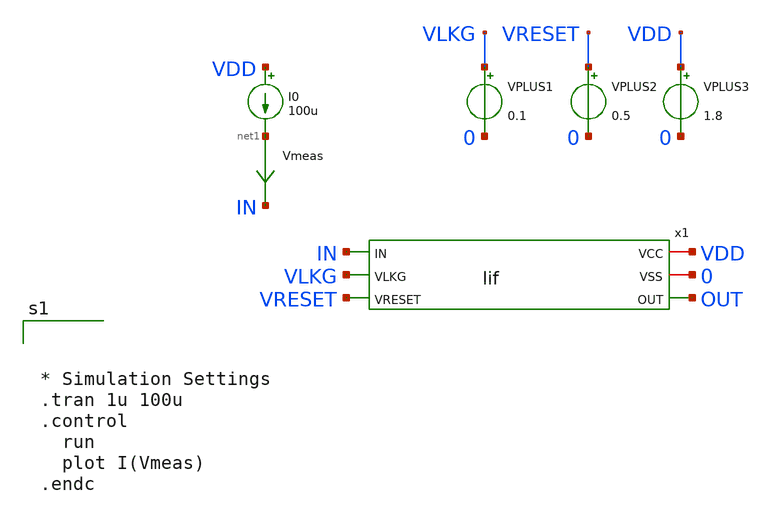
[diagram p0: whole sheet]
** sch_path: xschem/tb_lif.sch
**.subckt tb_lif
VPLUS1 VLKG 0 0.1
VPLUS2 VRESET 0 0.5
VPLUS3 VDD 0 1.8
x1 VDD 0 IN OUT VLKG VRESET lif
I0 VDD net1 100u
Vmeas net1 IN 0
.save i(vmeas)
**** begin user architecture code

** opencircuitdesign pdks install
.lib $::SKYWATER_MODELS/sky130.lib.spice tt





* Simulation Settings
.tran 1u 100u
.control
  run
  plot I(Vmeas)
.endc


**** end user architecture code
**.ends

* expanding   symbol:  lif.sym # of pins=6
** sym_path: xschem/lif.sym
** sch_path: xschem/lif.sch
.subckt lif VCC VSS IN OUT VLKG VRESET
*.iopin VCC
*.iopin VSS
*.ipin IN
*.opin OUT
*.ipin VLKG
*.ipin VRESET
XM1 IN VLKG VSS VSS sky130_fd_pr__nfet_01v8 L=0.15 W=1 nf=1 ad='int((nf+1)/2) * W/nf * 0.29' as='int((nf+2)/2) * W/nf * 0.29'
+ pd='2*int((nf+1)/2) * (W/nf + 0.29)' ps='2*int((nf+2)/2) * (W/nf + 0.29)' nrd='0.29 / W' nrs='0.29 / W'
+ sa=0 sb=0 sd=0 mult=1 m=1
XM2 IN OUT VRESET VSS sky130_fd_pr__nfet_01v8 L=0.15 W=1 nf=1 ad='int((nf+1)/2) * W/nf * 0.29' as='int((nf+2)/2) * W/nf * 0.29'
+ pd='2*int((nf+1)/2) * (W/nf + 0.29)' ps='2*int((nf+2)/2) * (W/nf + 0.29)' nrd='0.29 / W' nrs='0.29 / W'
+ sa=0 sb=0 sd=0 mult=1 m=1
XC1 IN VSS sky130_fd_pr__cap_mim_m3_1 W=1 L=1 MF=12 m=12
x1 VCC VSS OUT IN schmitt_trigger
.ends


* expanding   symbol:  /home/ahmadjabar/tugasakhir/xschem/schmitt_trigger.sym # of pins=4
** sym_path: xschem/schmitt_trigger.sym
** sch_path: xschem/schmitt_trigger.sch
.subckt schmitt_trigger VCC VSS OUT IN
*.ipin IN
*.opin OUT
*.iopin VCC
*.iopin VSS
XM1 net2 IN VCC VCC sky130_fd_pr__pfet_01v8 L=0.15 W=1 nf=1 ad='int((nf+1)/2) * W/nf * 0.29' as='int((nf+2)/2) * W/nf * 0.29'
+ pd='2*int((nf+1)/2) * (W/nf + 0.29)' ps='2*int((nf+2)/2) * (W/nf + 0.29)' nrd='0.29 / W' nrs='0.29 / W'
+ sa=0 sb=0 sd=0 mult=1 m=1
XM2 net3 IN net2 VCC sky130_fd_pr__pfet_01v8 L=0.15 W=1 nf=1 ad='int((nf+1)/2) * W/nf * 0.29' as='int((nf+2)/2) * W/nf * 0.29'
+ pd='2*int((nf+1)/2) * (W/nf + 0.29)' ps='2*int((nf+2)/2) * (W/nf + 0.29)' nrd='0.29 / W' nrs='0.29 / W'
+ sa=0 sb=0 sd=0 mult=1 m=1
XM3 net3 IN net1 VSS sky130_fd_pr__nfet_01v8 L=0.15 W=1 nf=1 ad='int((nf+1)/2) * W/nf * 0.29' as='int((nf+2)/2) * W/nf * 0.29'
+ pd='2*int((nf+1)/2) * (W/nf + 0.29)' ps='2*int((nf+2)/2) * (W/nf + 0.29)' nrd='0.29 / W' nrs='0.29 / W'
+ sa=0 sb=0 sd=0 mult=1 m=1
XM4 net1 IN VSS VSS sky130_fd_pr__nfet_01v8 L=0.15 W=1 nf=1 ad='int((nf+1)/2) * W/nf * 0.29' as='int((nf+2)/2) * W/nf * 0.29'
+ pd='2*int((nf+1)/2) * (W/nf + 0.29)' ps='2*int((nf+2)/2) * (W/nf + 0.29)' nrd='0.29 / W' nrs='0.29 / W'
+ sa=0 sb=0 sd=0 mult=1 m=1
XM5 VSS net3 net2 VCC sky130_fd_pr__pfet_01v8 L=0.15 W=1 nf=1 ad='int((nf+1)/2) * W/nf * 0.29' as='int((nf+2)/2) * W/nf * 0.29'
+ pd='2*int((nf+1)/2) * (W/nf + 0.29)' ps='2*int((nf+2)/2) * (W/nf + 0.29)' nrd='0.29 / W' nrs='0.29 / W'
+ sa=0 sb=0 sd=0 mult=1 m=1
XM6 VCC net3 net1 VSS sky130_fd_pr__nfet_01v8 L=0.15 W=1 nf=1 ad='int((nf+1)/2) * W/nf * 0.29' as='int((nf+2)/2) * W/nf * 0.29'
+ pd='2*int((nf+1)/2) * (W/nf + 0.29)' ps='2*int((nf+2)/2) * (W/nf + 0.29)' nrd='0.29 / W' nrs='0.29 / W'
+ sa=0 sb=0 sd=0 mult=1 m=1
XM7 OUT net3 VSS VSS sky130_fd_pr__nfet_01v8 L=0.15 W=1 nf=1 ad='int((nf+1)/2) * W/nf * 0.29' as='int((nf+2)/2) * W/nf * 0.29'
+ pd='2*int((nf+1)/2) * (W/nf + 0.29)' ps='2*int((nf+2)/2) * (W/nf + 0.29)' nrd='0.29 / W' nrs='0.29 / W'
+ sa=0 sb=0 sd=0 mult=1 m=1
XM8 OUT net3 VCC VCC sky130_fd_pr__pfet_01v8 L=0.15 W=1 nf=1 ad='int((nf+1)/2) * W/nf * 0.29' as='int((nf+2)/2) * W/nf * 0.29'
+ pd='2*int((nf+1)/2) * (W/nf + 0.29)' ps='2*int((nf+2)/2) * (W/nf + 0.29)' nrd='0.29 / W' nrs='0.29 / W'
+ sa=0 sb=0 sd=0 mult=1 m=1
.ends

.end
